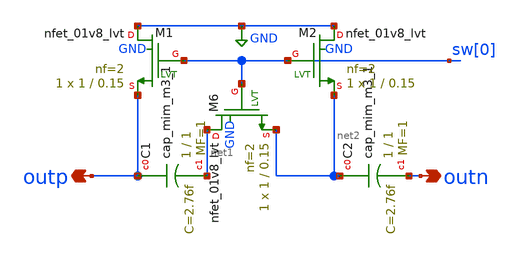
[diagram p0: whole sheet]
** sch_path: openfasoc/generators/lc-dco/xschem_rundir/untitled.sch
**.subckt untitled outn outp
*.opin outn
*.opin outp
XC1 outp net1 sky130_fd_pr__cap_mim_m3_1 W=1 L=1 MF=1 m=1
XC2 net2 outn sky130_fd_pr__cap_mim_m3_1 W=1 L=1 MF=1 m=1
XM6 net1 sw[0] net2 GND sky130_fd_pr__nfet_01v8_lvt L=0.15 W=1 nf=2 ad='int((nf+1)/2) * W/nf * 0.29'
+ as='int((nf+2)/2) * W/nf * 0.29' pd='2*int((nf+1)/2) * (W/nf + 0.29)' ps='2*int((nf+2)/2) * (W/nf + 0.29)'
+ nrd='0.29 / W' nrs='0.29 / W' sa=0 sb=0 sd=0 mult=1 m=1
XM1 GND sw[0] outp GND sky130_fd_pr__nfet_01v8_lvt L=0.15 W=1 nf=2 ad='int((nf+1)/2) * W/nf * 0.29' as='int((nf+2)/2) * W/nf * 0.29'
+ pd='2*int((nf+1)/2) * (W/nf + 0.29)' ps='2*int((nf+2)/2) * (W/nf + 0.29)' nrd='0.29 / W' nrs='0.29 / W'
+ sa=0 sb=0 sd=0 mult=1 m=1
XM2 GND sw[0] net2 GND sky130_fd_pr__nfet_01v8_lvt L=0.15 W=1 nf=2 ad='int((nf+1)/2) * W/nf * 0.29' as='int((nf+2)/2) * W/nf * 0.29'
+ pd='2*int((nf+1)/2) * (W/nf + 0.29)' ps='2*int((nf+2)/2) * (W/nf + 0.29)' nrd='0.29 / W' nrs='0.29 / W'
+ sa=0 sb=0 sd=0 mult=1 m=1
**.ends
.GLOBAL GND
.end
